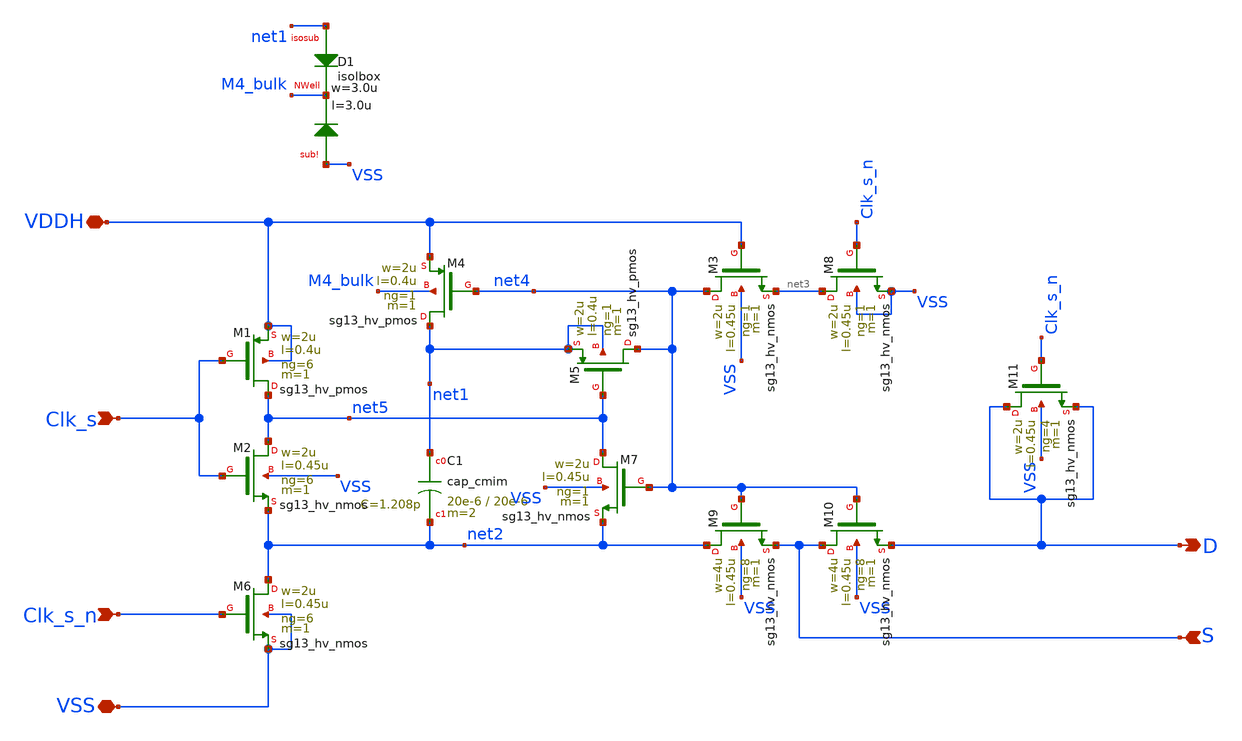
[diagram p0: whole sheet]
** sch_path: sar_adc/xschem/blocks/bootstrapped_sw/bs_switch_hv.sch
**.subckt bs_switch_hv Clk_s Clk_s_n S VDDH VSS D
*.ipin Clk_s
*.ipin Clk_s_n
*.ipin S
*.iopin VDDH
*.iopin VSS
*.opin D
XC1 net1 net2 cap_cmim w=20e-6 l=20e-6 m=2 mm_ok=1
XM1 net5 Clk_s VDDH VDDH sg13_hv_pmos w=2u l=0.4u ng=6 m=1 mm_ok=1
XM2 net5 Clk_s net2 VSS sg13_hv_nmos w=2u l=0.45u ng=6 m=1 mm_ok=1
XM6 net2 Clk_s_n VSS VSS sg13_hv_nmos w=2u l=0.45u ng=6 m=1 mm_ok=1
XM4 net1 net4 VDDH M4_bulk sg13_hv_pmos w=2u l=0.4u ng=1 m=1 mm_ok=1
XM5 net4 net5 net1 net1 sg13_hv_pmos w=2u l=0.4u ng=1 m=1 mm_ok=1
XM7 net5 net4 net2 VSS sg13_hv_nmos w=2u l=0.45u ng=1 m=1 mm_ok=1
XM3 net4 VDDH net3 VSS sg13_hv_nmos w=2u l=0.45u ng=1 m=1 mm_ok=1
XM8 net3 Clk_s_n VSS VSS sg13_hv_nmos w=2u l=0.45u ng=1 m=1 mm_ok=1
XM9 net2 net4 S VSS sg13_hv_nmos w=4u l=0.45u ng=8 m=1 mm_ok=1
XM10 S net4 D VSS sg13_hv_nmos w=4u l=0.45u ng=8 m=1 mm_ok=1
XD1 net1 M4_bulk VSS isolbox l=3.0u w=3.0u
XM11 D Clk_s_n D VSS sg13_hv_nmos w=2u l=0.45u ng=4 m=1 mm_ok=1
**.ends
.end
